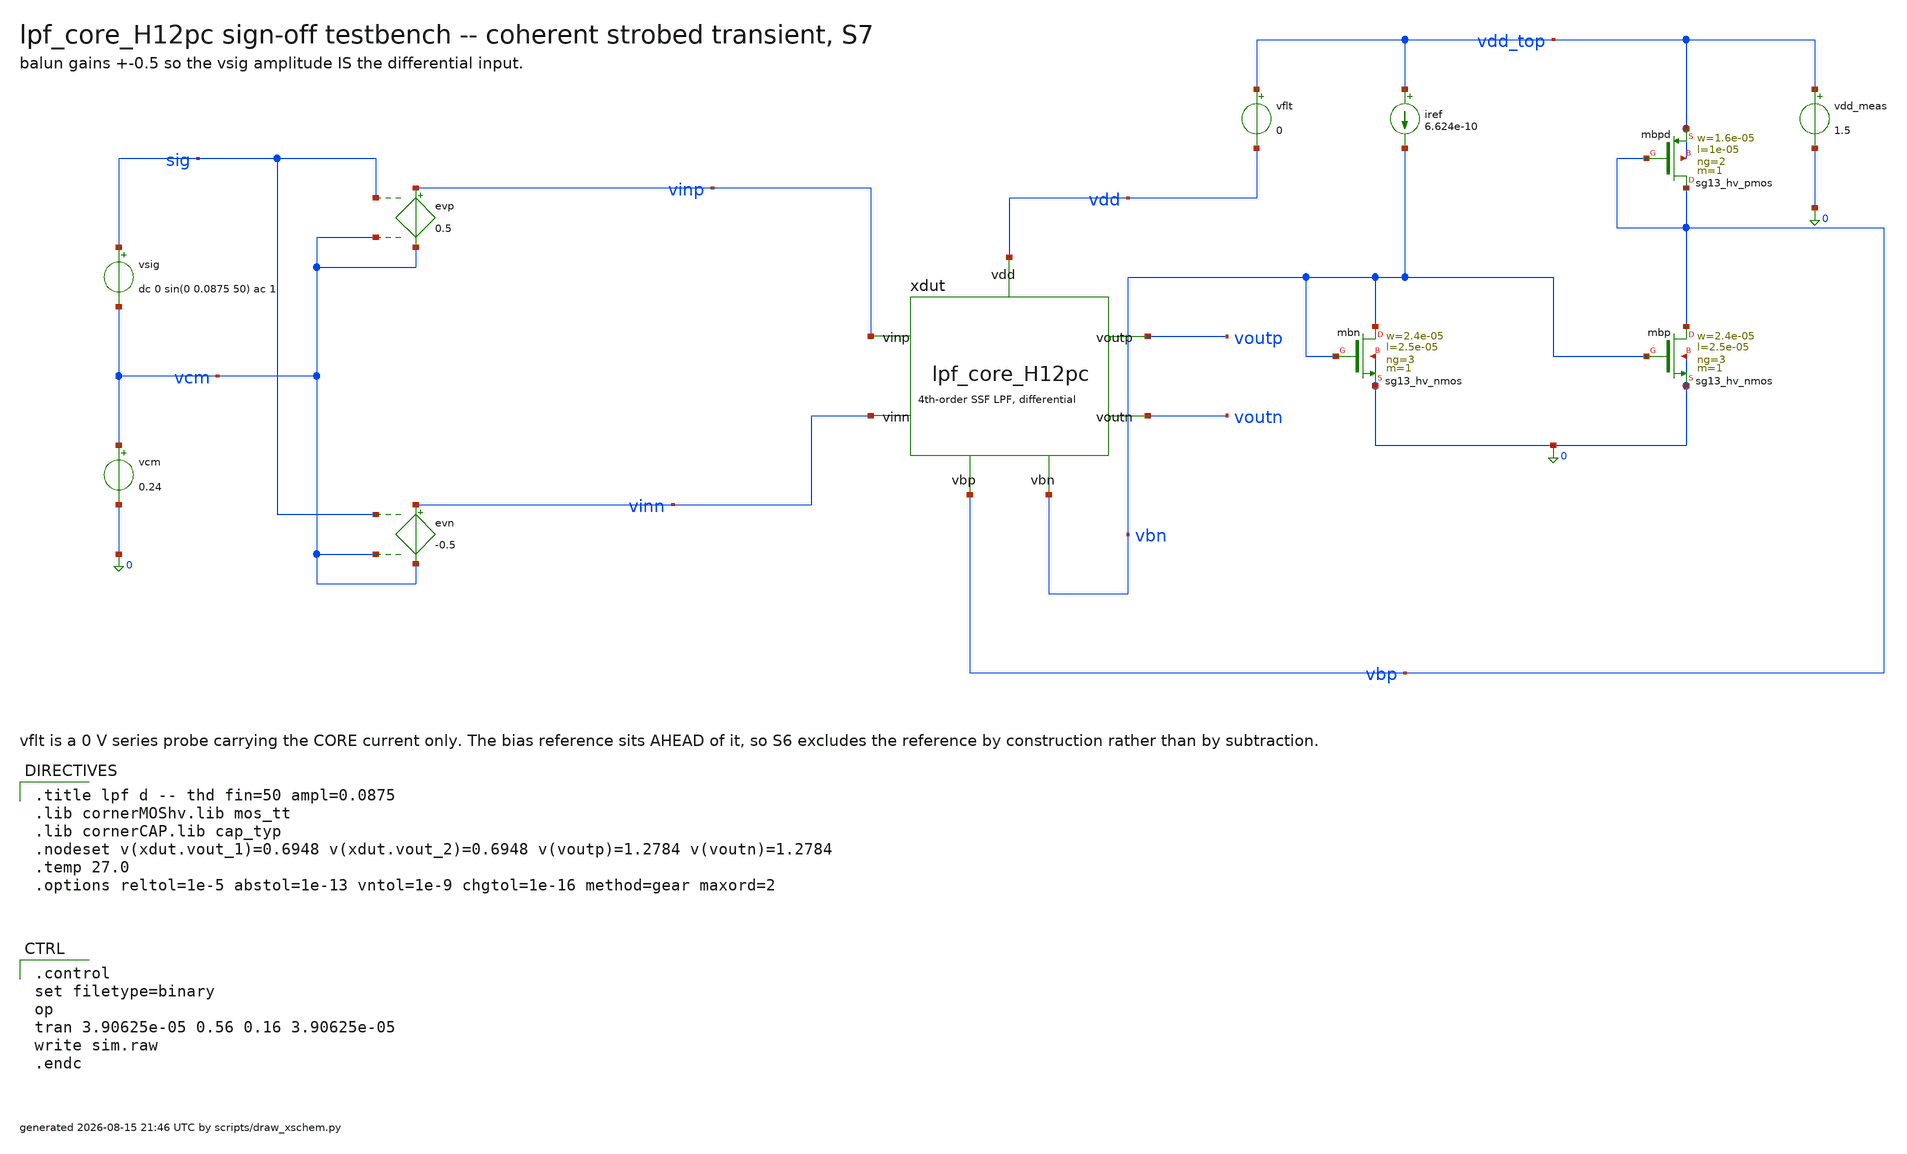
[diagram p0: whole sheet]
** sch_path: signoff/post-pvt/H12-pdk-cap/lpf_tb_H12pc_thd.sch
**.subckt lpf_tb_H12pc_thd
vsig sig vcm dc 0 sin(0 0.0875 50) ac 1
vcm vcm 0 0.24
evp vinp vcm sig vcm 0.5
evn vinn vcm sig vcm -0.5
xdut vinp vinn voutp voutn vbn vbp vdd lpf_core_H12pc
vflt vdd_top vdd 0
vdd_meas vdd_top 0 1.5
iref vdd_top vbn 6.624e-10
Xmbn vbn vbn 0 0 sg13_hv_nmos w=2.4e-05 l=2.5e-05 ng=3 m=1 mm_ok=1
Xmbp vbp vbn 0 0 sg13_hv_nmos w=2.4e-05 l=2.5e-05 ng=3 m=1 mm_ok=1
Xmbpd vbp vbp vdd_top vdd_top sg13_hv_pmos w=1.6e-05 l=1e-05 ng=2 m=1 mm_ok=1
**** begin user architecture code

.title lpf d -- thd fin=50 ampl=0.0875
.lib cornerMOShv.lib mos_tt
.lib cornerCAP.lib cap_typ
.nodeset v(xdut.vout_1)=0.6948 v(xdut.vout_2)=0.6948 v(voutp)=1.2784 v(voutn)=1.2784
.temp 27.0
.options reltol=1e-5 abstol=1e-13 vntol=1e-9 chgtol=1e-16 method=gear maxord=2


.control
set filetype=binary
op
tran 3.90625e-05 0.56 0.16 3.90625e-05
write sim.raw
.endc

**** end user architecture code
**.ends

* expanding   symbol:  lpf_core_H12pc.sym # of pins=7
** sym_path: signoff/post-pvt/H12-pdk-cap/lpf_core_H12pc.sym
** sch_path: signoff/post-pvt/H12-pdk-cap/lpf_core_H12pc.sch
.subckt lpf_core_H12pc vinp vinn voutp voutn vbn vbp vdd
*.ipin vinp
*.ipin vinn
*.opin voutp
*.opin voutn
*.ipin vdd
*.ipin vbn
*.ipin vbp
Xm2 net2 vinp vout_1 vout_1 sg13_hv_pmos w=1.6e-05 l=1e-05 ng=2 m=1 mm_ok=1
Xm5 net3 vinn vout_2 vout_2 sg13_hv_pmos w=1.6e-05 l=1e-05 ng=2 m=1 mm_ok=1
Xm4 vout_1 net2 0 0 sg13_hv_nmos w=1.5e-06 l=4.5e-05 ng=1 m=1 mm_ok=1
Xm8 vout_2 net3 0 0 sg13_hv_nmos w=1.5e-06 l=4.5e-05 ng=1 m=1 mm_ok=1
Xm9 net2 vbn 0 0 sg13_hv_nmos w=2.4e-05 l=2.5e-05 ng=3 m=1 mm_ok=1
Xm10 net3 vbn 0 0 sg13_hv_nmos w=2.4e-05 l=2.5e-05 ng=3 m=1 mm_ok=1
Xmst vout_1 vbr net4 net4 sg13_hv_pmos w=5e-06 l=3.3e-05 ng=1 m=1 mm_ok=1
Xmstn vout_2 vbr net1 net1 sg13_hv_pmos w=5e-06 l=3.3e-05 ng=1 m=1 mm_ok=1
Xm0 net4 vout_1 voutp voutp sg13_hv_pmos w=4e-06 l=1.5e-05 ng=1 m=1 mm_ok=1
Xm1 net1 vout_2 voutn voutn sg13_hv_pmos w=4e-06 l=1.5e-05 ng=1 m=1 mm_ok=1
Xm14 voutp net4 vdd vdd sg13_hv_pmos w=1.2e-05 l=3.1e-05 ng=2 m=1 mm_ok=1
Xm15 voutn net1 vdd vdd sg13_hv_pmos w=1.2e-05 l=3.1e-05 ng=2 m=1 mm_ok=1
Xr1 rep_x rep_x vdd vdd sg13_hv_pmos w=1.2e-05 l=3.1e-05 ng=2 m=1 mm_ok=1
Xr2 vbr vbr rep_x rep_x sg13_hv_pmos w=5e-06 l=3.3e-05 ng=1 m=1 mm_ok=1
Xr3 vbr vbn 0 0 sg13_hv_nmos w=2.4e-05 l=2.5e-05 ng=3 m=4 mm_ok=1
Xc13 net2 vout_1 cap_cmim w=40.53u l=40.53u m=2 mm_ok=1
Xc17 net3 vout_2 cap_cmim w=40.53u l=40.53u m=2 mm_ok=1
Xc19 vout_2 vout_1 cap_cmim w=49.42u l=49.42u m=8 mm_ok=1
Xc1 voutp net4 cap_cmim w=49.91u l=49.91u m=16 mm_ok=1
Xc10 voutn net1 cap_cmim w=49.91u l=49.91u m=16 mm_ok=1
Xc12 voutn voutp cap_cmim w=48.45u l=48.45u m=7 mm_ok=1
.ends

.end
